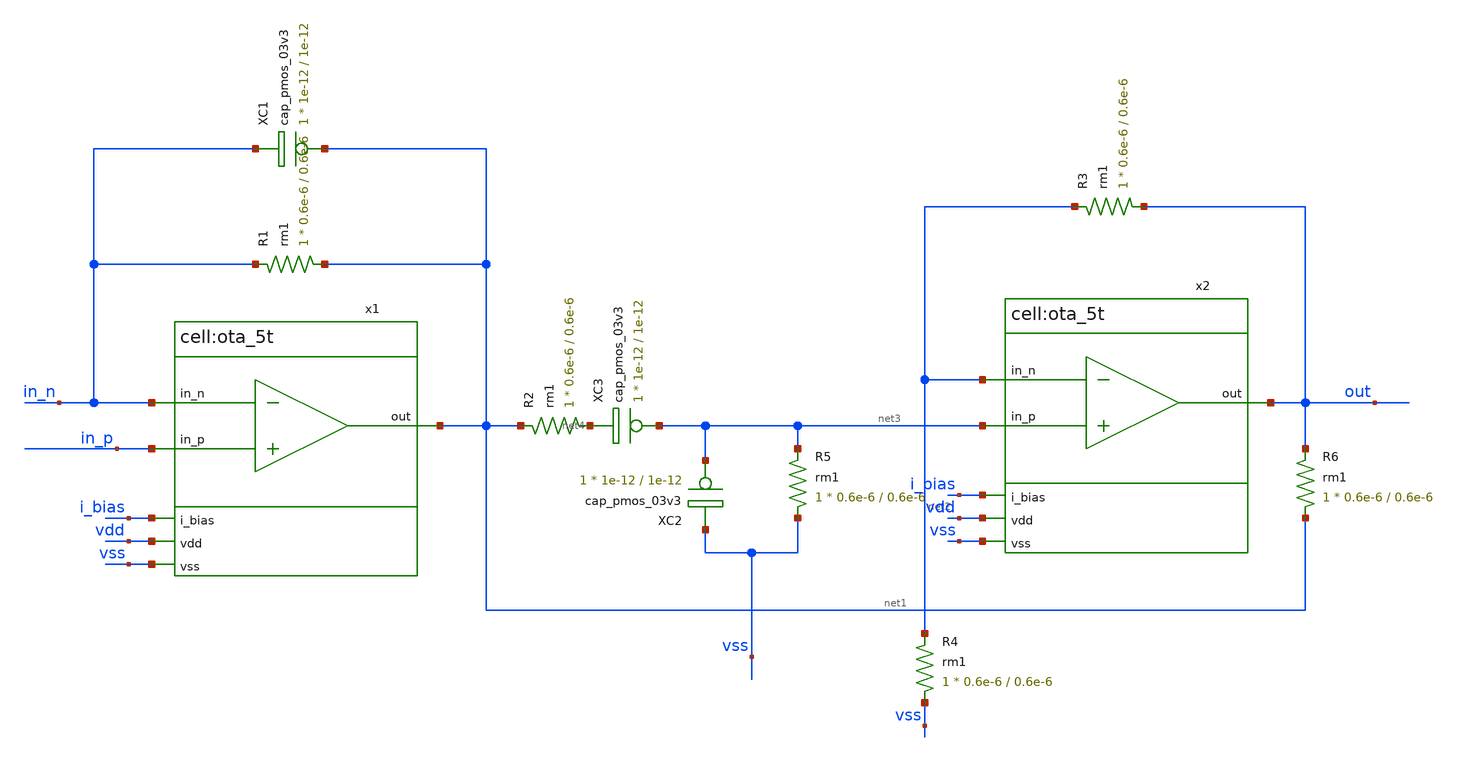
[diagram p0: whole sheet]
** sch_path: Analog/schematics/1_readout/bpf/Transimpedance_AmplifierwBandFilter.sch
**.subckt Transimpedance_AmplifierwBandFilter
x1 vdd net1 in_p in_n i_bias vss ota_5t
XC1 net1 in_n cap_pmos_03v3 c_width=1e-12 c_length=1e-12 m=1
XR1 net1 in_n rm1 r_width=0.6e-6 r_length=0.6e-6 m=1
x2 vdd out net3 net2 i_bias vss ota_5t
XR2 net4 net1 rm1 r_width=0.6e-6 r_length=0.6e-6 m=1
XR3 out net2 rm1 r_width=0.6e-6 r_length=0.6e-6 m=1
XR4 vss net2 rm1 r_width=0.6e-6 r_length=0.6e-6 m=1
XC2 net3 vss cap_pmos_03v3 c_width=1e-12 c_length=1e-12 m=1
XR5 vss net3 rm1 r_width=0.6e-6 r_length=0.6e-6 m=1
XC3 net3 net4 cap_pmos_03v3 c_width=1e-12 c_length=1e-12 m=1
XR6 net1 out rm1 r_width=0.6e-6 r_length=0.6e-6 m=1
**.ends

* expanding   symbol:  core_analog/ota_5t/ota_5t.sym # of pins=6
** sym_path: core_analog/ota_5t/ota_5t.sym
** sch_path: core_analog/ota_5t/ota_5t.sch
.subckt ota_5t vdd out in_p in_n i_bias vss
*.ipin in_p
*.ipin in_n
*.ipin i_bias
*.ipin vdd
*.ipin vss
*.opin out
XM1 net2 i_bias vss vss nfet_03v3 L=0.28u W=6u nf=2 ad='int((nf+1)/2) * W/nf * 0.18u' as='int((nf+2)/2) * W/nf * 0.18u'
+ pd='2*int((nf+1)/2) * (W/nf + 0.18u)' ps='2*int((nf+2)/2) * (W/nf + 0.18u)' nrd='0.18u / W' nrs='0.18u / W'
+ sa=0 sb=0 sd=0 m=2
XM2 i_bias i_bias vss vss nfet_03v3 L=0.28u W=6u nf=2 ad='int((nf+1)/2) * W/nf * 0.18u' as='int((nf+2)/2) * W/nf * 0.18u'
+ pd='2*int((nf+1)/2) * (W/nf + 0.18u)' ps='2*int((nf+2)/2) * (W/nf + 0.18u)' nrd='0.18u / W' nrs='0.18u / W'
+ sa=0 sb=0 sd=0 m=1
XM3 net1 in_p net2 vss nfet_03v3 L=0.28u W=6u nf=2 ad='int((nf+1)/2) * W/nf * 0.18u' as='int((nf+2)/2) * W/nf * 0.18u'
+ pd='2*int((nf+1)/2) * (W/nf + 0.18u)' ps='2*int((nf+2)/2) * (W/nf + 0.18u)' nrd='0.18u / W' nrs='0.18u / W'
+ sa=0 sb=0 sd=0 m=1
XM4 out in_n net2 vss nfet_03v3 L=0.28u W=6u nf=2 ad='int((nf+1)/2) * W/nf * 0.18u' as='int((nf+2)/2) * W/nf * 0.18u'
+ pd='2*int((nf+1)/2) * (W/nf + 0.18u)' ps='2*int((nf+2)/2) * (W/nf + 0.18u)' nrd='0.18u / W' nrs='0.18u / W'
+ sa=0 sb=0 sd=0 m=1
XM5 out net1 vdd vdd pfet_03v3 L=0.28u W=6u nf=2 ad='int((nf+1)/2) * W/nf * 0.18u' as='int((nf+2)/2) * W/nf * 0.18u'
+ pd='2*int((nf+1)/2) * (W/nf + 0.18u)' ps='2*int((nf+2)/2) * (W/nf + 0.18u)' nrd='0.18u / W' nrs='0.18u / W'
+ sa=0 sb=0 sd=0 m=3
XM6 net1 net1 vdd vdd pfet_03v3 L=0.28u W=6u nf=2 ad='int((nf+1)/2) * W/nf * 0.18u' as='int((nf+2)/2) * W/nf * 0.18u'
+ pd='2*int((nf+1)/2) * (W/nf + 0.18u)' ps='2*int((nf+2)/2) * (W/nf + 0.18u)' nrd='0.18u / W' nrs='0.18u / W'
+ sa=0 sb=0 sd=0 m=3
.ends

.end
